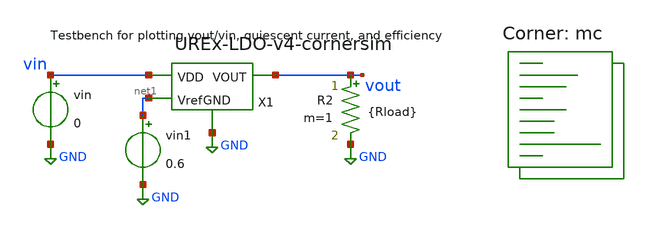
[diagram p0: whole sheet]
** sch_path: xschem/corner-sims/VoutvsVin-v4-cornersim.sch
**.subckt VoutvsVin-v4-cornersim
vin vin GND 0
R2 vout GND {Rload} m=1
X1 vin vout GND net1 UREx-LDO-v4-cornersim
vin1 net1 GND 0.6
**** begin user architecture code


.param mc_mm_switch=1
.param mc_pr_switch=1
.param Rload=20
.control
  dc vin 0.5 5 0.1
  wrdata mc_out.csv v(vin) v(vout)

  set appendwrite

  repeat 100
    reset
    dc vin 0.5 5 0.1
    wrdata mc_out.csv v(vin) v(vout)
  end
.endc


.lib $::SKYWATER_MODELS/sky130.lib.spice mc
**** end user architecture code
**.ends

* expanding   symbol:  UREx-LDO-v4-cornersim.sym # of pins=4
** sym_path: xschem/UREx-LDO-v4-cornersim.sym
** sch_path: xschem/UREx-LDO-v4-cornersim.sch
.subckt UREx-LDO-v4-cornersim VDD VOUT GND Vref
*.ipin VDD
*.opin VOUT
*.ipin GND
*.ipin Vref
XM1 net3 Vref net1 GND sky130_fd_pr__nfet_01v8_lvt L=1 W=0.8 nf=1 ad='int((1 + 1)/2) * 0.8 / 1 * 0.29'
+ as='int((1 + 2)/2) * 0.8 / 1 * 0.29' pd='2*int((1 + 1)/2) * (0.8 / 1 + 0.29)' ps='2*int((1 + 2)/2) * (0.8 / 1 + 0.29)'
+ nrd='0.29 / 0.8 ' nrs='0.29 / 0.8 ' sa=0 sb=0 sd=0 mult=1 m=1
XM2 net2 v+ net1 GND sky130_fd_pr__nfet_01v8_lvt L=1 W=0.8 nf=1 ad='int((1 + 1)/2) * 0.8 / 1 * 0.29'
+ as='int((1 + 2)/2) * 0.8 / 1 * 0.29' pd='2*int((1 + 1)/2) * (0.8 / 1 + 0.29)' ps='2*int((1 + 2)/2) * (0.8 / 1 + 0.29)'
+ nrd='0.29 / 0.8 ' nrs='0.29 / 0.8 ' sa=0 sb=0 sd=0 mult=1 m=1
XM4 net2 net3 VDD VDD sky130_fd_pr__pfet_01v8_lvt L=1 W=0.5 nf=1 ad='int((1 + 1)/2) * 0.5 / 1 * 0.29'
+ as='int((1 + 2)/2) * 0.5 / 1 * 0.29' pd='2*int((1 + 1)/2) * (0.5 / 1 + 0.29)' ps='2*int((1 + 2)/2) * (0.5 / 1 + 0.29)'
+ nrd='0.29 / 0.5 ' nrs='0.29 / 0.5 ' sa=0 sb=0 sd=0 mult=1 m=1
XM3 net3 net3 VDD VDD sky130_fd_pr__pfet_01v8_lvt L=1 W=0.5 nf=1 ad='int((1 + 1)/2) * 0.5 / 1 * 0.29'
+ as='int((1 + 2)/2) * 0.5 / 1 * 0.29' pd='2*int((1 + 1)/2) * (0.5 / 1 + 0.29)' ps='2*int((1 + 2)/2) * (0.5 / 1 + 0.29)'
+ nrd='0.29 / 0.5 ' nrs='0.29 / 0.5 ' sa=0 sb=0 sd=0 mult=1 m=1
XM6 gate net2 VDD VDD sky130_fd_pr__pfet_01v8_lvt L=0.35 W=4.2 nf=1 ad='int((1 + 1)/2) * 4.2 / 1 * 0.29'
+ as='int((1 + 2)/2) * 4.2 / 1 * 0.29' pd='2*int((1 + 1)/2) * (4.2 / 1 + 0.29)' ps='2*int((1 + 2)/2) * (4.2 / 1 + 0.29)'
+ nrd='0.29 / 4.2 ' nrs='0.29 / 4.2 ' sa=0 sb=0 sd=0 mult=1 m=1
XM7 gate net4 GND GND sky130_fd_pr__nfet_01v8_lvt L=0.25 W=5.2 nf=1 ad='int((1 + 1)/2) * 5.2 / 1 * 0.29'
+ as='int((1 + 2)/2) * 5.2 / 1 * 0.29' pd='2*int((1 + 1)/2) * (5.2 / 1 + 0.29)' ps='2*int((1 + 2)/2) * (5.2 / 1 + 0.29)'
+ nrd='0.29 / 5.2 ' nrs='0.29 / 5.2 ' sa=0 sb=0 sd=0 mult=1 m=1
XM9 VOUT gate VDD VDD sky130_fd_pr__pfet_01v8_lvt L=0.35 W=35 nf=1 ad='int((1 + 1)/2) * 35 / 1 * 0.29'
+ as='int((1 + 2)/2) * 35 / 1 * 0.29' pd='2*int((1 + 1)/2) * (35 / 1 + 0.29)' ps='2*int((1 + 2)/2) * (35 / 1 + 0.29)'
+ nrd='0.29 / 35 ' nrs='0.29 / 35 ' sa=0 sb=0 sd=0 mult=50 m=50
XM10 net4 net5 VDD VDD sky130_fd_pr__pfet_01v8_lvt L=1 W=1 nf=1 ad='int((1 + 1)/2) * 1 / 1 * 0.29' as='int((1 + 2)/2) * 1 / 1 * 0.29'
+ pd='2*int((1 + 1)/2) * (1 / 1 + 0.29)' ps='2*int((1 + 2)/2) * (1 / 1 + 0.29)' nrd='0.29 / 1 ' nrs='0.29 / 1 '
+ sa=0 sb=0 sd=0 mult=1 m=1
XM11 net5 net5 VDD VDD sky130_fd_pr__pfet_01v8_lvt L=1 W=1 nf=1 ad='int((1 + 1)/2) * 1 / 1 * 0.29' as='int((1 + 2)/2) * 1 / 1 * 0.29'
+ pd='2*int((1 + 1)/2) * (1 / 1 + 0.29)' ps='2*int((1 + 2)/2) * (1 / 1 + 0.29)' nrd='0.29 / 1 ' nrs='0.29 / 1 '
+ sa=0 sb=0 sd=0 mult=1 m=1
XM12 net7 net5 VDD VDD sky130_fd_pr__pfet_01v8_lvt L=1 W=1 nf=1 ad='int((1 + 1)/2) * 1 / 1 * 0.29' as='int((1 + 2)/2) * 1 / 1 * 0.29'
+ pd='2*int((1 + 1)/2) * (1 / 1 + 0.29)' ps='2*int((1 + 2)/2) * (1 / 1 + 0.29)' nrd='0.29 / 1 ' nrs='0.29 / 1 '
+ sa=0 sb=0 sd=0 mult=1 m=1
XM13 net7 net7 GND GND sky130_fd_pr__nfet_01v8_lvt L=1 W=2 nf=1 ad='int((1 + 1)/2) * 2 / 1 * 0.29' as='int((1 + 2)/2) * 2 / 1 * 0.29'
+ pd='2*int((1 + 1)/2) * (2 / 1 + 0.29)' ps='2*int((1 + 2)/2) * (2 / 1 + 0.29)' nrd='0.29 / 2 ' nrs='0.29 / 2 '
+ sa=0 sb=0 sd=0 mult=1 m=1
XM14 net5 net7 net6 net6 sky130_fd_pr__nfet_01v8_lvt L=1 W=2.2 nf=1 ad='int((1 + 1)/2) * 2.2 / 1 * 0.29'
+ as='int((1 + 2)/2) * 2.2 / 1 * 0.29' pd='2*int((1 + 1)/2) * (2.2 / 1 + 0.29)' ps='2*int((1 + 2)/2) * (2.2 / 1 + 0.29)'
+ nrd='0.29 / 2.2 ' nrs='0.29 / 2.2 ' sa=0 sb=0 sd=0 mult=1 m=1
XR1 v+ VOUT GND sky130_fd_pr__res_high_po_0p35 L=35.7 mult=1 m=1
XR3 GND v+ GND sky130_fd_pr__res_high_po_0p35 L=53.9 mult=1 m=1
XR2 GND net6 GND sky130_fd_pr__res_high_po_0p35 L=3.1 mult=1 m=1
XC1 gate net2 sky130_fd_pr__cap_mim_m3_1 W=50 L=50 MF=1 m=1
XM5 net1 net4 GND GND sky130_fd_pr__nfet_01v8_lvt L=1 W=1.2 nf=1 ad='int((1 + 1)/2) * 1.2 / 1 * 0.29'
+ as='int((1 + 2)/2) * 1.2 / 1 * 0.29' pd='2*int((1 + 1)/2) * (1.2 / 1 + 0.29)' ps='2*int((1 + 2)/2) * (1.2 / 1 + 0.29)'
+ nrd='0.29 / 1.2 ' nrs='0.29 / 1.2 ' sa=0 sb=0 sd=0 mult=1 m=1
XM8 net4 net4 GND GND sky130_fd_pr__nfet_01v8_lvt L=1 W=1.2 nf=1 ad='int((1 + 1)/2) * 1.2 / 1 * 0.29'
+ as='int((1 + 2)/2) * 1.2 / 1 * 0.29' pd='2*int((1 + 1)/2) * (1.2 / 1 + 0.29)' ps='2*int((1 + 2)/2) * (1.2 / 1 + 0.29)'
+ nrd='0.29 / 1.2 ' nrs='0.29 / 1.2 ' sa=0 sb=0 sd=0 mult=1 m=1
.ends

.GLOBAL GND
.end
